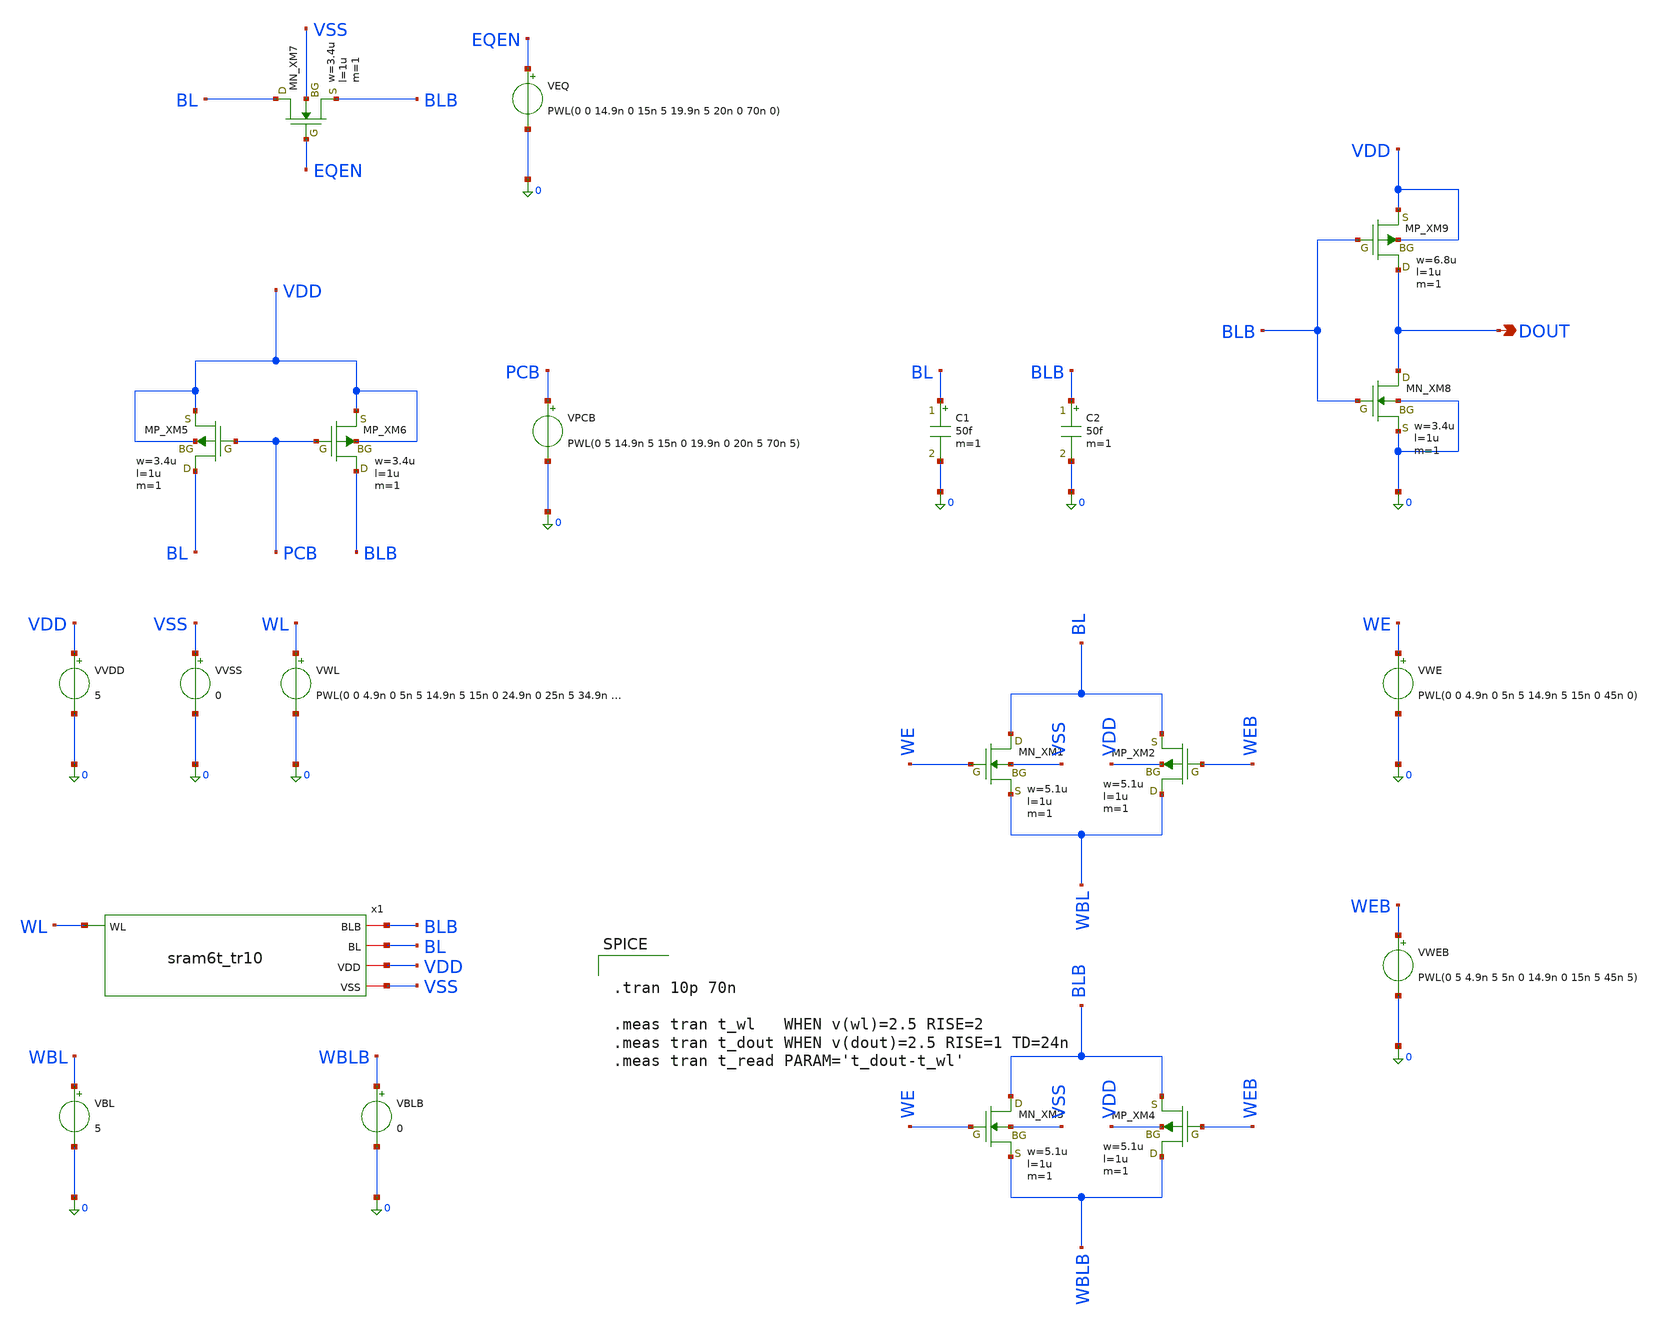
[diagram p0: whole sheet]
** sch_path: cell/tb_read_buffer.sch
**.subckt tb_read_buffer DOUT
*.opin DOUT
VVDD VDD 0 5
VWL WL 0 PWL(0 0 4.9n 0 5n 5 14.9n 5 15n 0 24.9n 0 25n 5 34.9n 5 35n 0 70n 0)
VBL WBL 0 5
VBLB WBLB 0 0
VVSS VSS 0 0
x1 BL BLB WL VDD VSS sram6t_tr10
XXM1 BL WE WBL VSS NMOS w=5.1u l=1u nrd=0 nrs=0 m=1
XXM2 WBL WEB BL VDD PMOS w=5.1u l=1u nrd=0 nrs=0 m=1
VWE WE 0 PWL(0 0 4.9n 0 5n 5 14.9n 5 15n 0 45n 0)
VWEB WEB 0 PWL(0 5 4.9n 5 5n 0 14.9n 0 15n 5 45n 5)
XXM3 BLB WE WBLB VSS NMOS w=5.1u l=1u nrd=0 nrs=0 m=1
XXM4 WBLB WEB BLB VDD PMOS w=5.1u l=1u nrd=0 nrs=0 m=1
XXM5 BL PCB VDD VDD PMOS w=3.4u l=1u nrd=0 nrs=0 m=1
XXM6 BLB PCB VDD VDD PMOS w=3.4u l=1u nrd=0 nrs=0 m=1
VPCB PCB 0 PWL(0 5 14.9n 5 15n 0 19.9n 0 20n 5 70n 5)
C1 BL 0 50f m=1
C2 BLB 0 50f m=1
XXM7 BL EQEN BLB VSS NMOS w=3.4u l=1u nrd=0 nrs=0 m=1
VEQ EQEN 0 PWL(0 0 14.9n 0 15n 5 19.9n 5 20n 0 70n 0)
XXM9 DOUT BLB VDD VDD PMOS w=6.8u l=1u nrd=0 nrs=0 m=1
XXM8 DOUT BLB 0 0 NMOS w=3.4u l=1u nrd=0 nrs=0 m=1
**** begin user architecture code
 .include $::LIB/ip62_models


.tran 10p 70n

.meas tran t_wl   WHEN v(wl)=2.5 RISE=2
.meas tran t_dout WHEN v(dout)=2.5 RISE=1 TD=24n
.meas tran t_read PARAM='t_dout-t_wl'


**** end user architecture code
**.ends
.end
